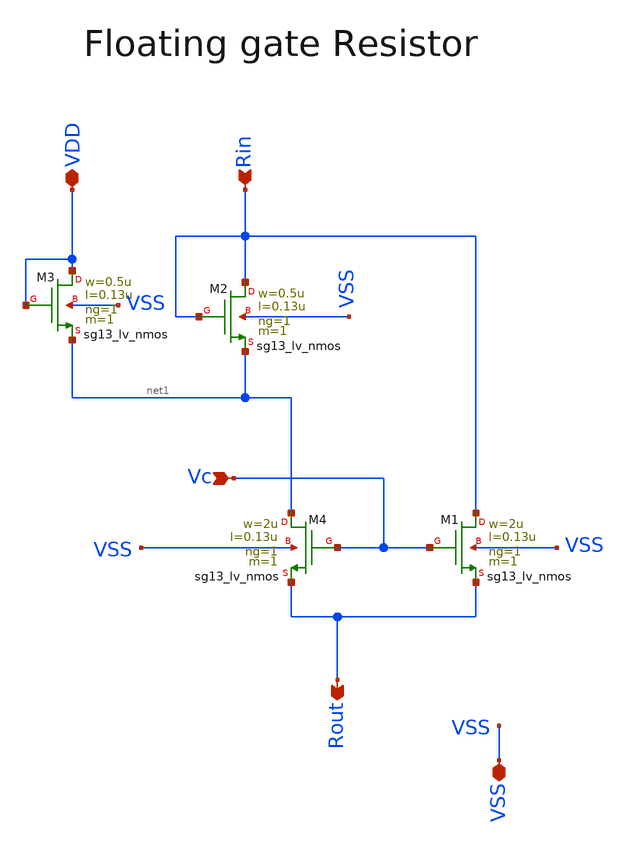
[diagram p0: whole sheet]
** sch_path: macros/heichips26_analog_project/macros/floating-gate/schematic/xschem/floating-gate.sch
**.subckt floating-gate VDD Rin Rout Vc VSS
*.iopin VDD
*.ipin Rin
*.opin Rout
*.ipin Vc
*.iopin VSS
XM1 Rin Vc Rout VSS sg13_lv_nmos w=2u l=0.13u ng=1 m=1 mm_ok=1
XM2 Rin Rin net1 VSS sg13_lv_nmos w=0.5u l=0.13u ng=1 m=1 mm_ok=1
XM3 VDD VDD net1 VSS sg13_lv_nmos w=0.5u l=0.13u ng=1 m=1 mm_ok=1
XM4 net1 Vc Rout VSS sg13_lv_nmos w=2u l=0.13u ng=1 m=1 mm_ok=1
**.ends
.end
